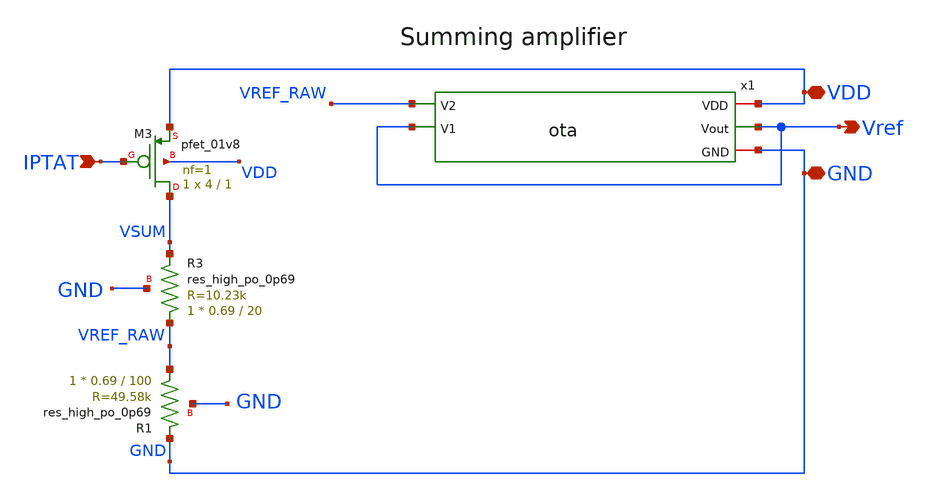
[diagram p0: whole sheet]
** sch_path: subcells/xschem/sumamp.sch
**.subckt sumamp IPTAT Vref VDD GND
*.ipin IPTAT
*.opin Vref
*.iopin VDD
*.iopin GND
XM3 VSUM IPTAT VDD VDD sky130_fd_pr__pfet_01v8 L=1 W=4 nf=1 ad='int((1 + 1)/2) * 4 / 1 * 0.29' as='int((1 + 2)/2) * 4 / 1 * 0.29'
+ pd='2*int((1 + 1)/2) * (4 / 1 + 0.29)' ps='2*int((1 + 2)/2) * (4 / 1 + 0.29)' nrd='0.29 / 4 ' nrs='0.29 / 4 '
+ sa=0 sb=0 sd=0 mult=1 m=1
XR1 VREF_RAW GND GND sky130_fd_pr__res_high_po_0p69 L=100 mult=1 m=1
XR3 VREF_RAW VSUM GND sky130_fd_pr__res_high_po_0p69 L=20 mult=1 m=1
x1 VDD VREF_RAW Vref Vref GND ota
**.ends
.end
